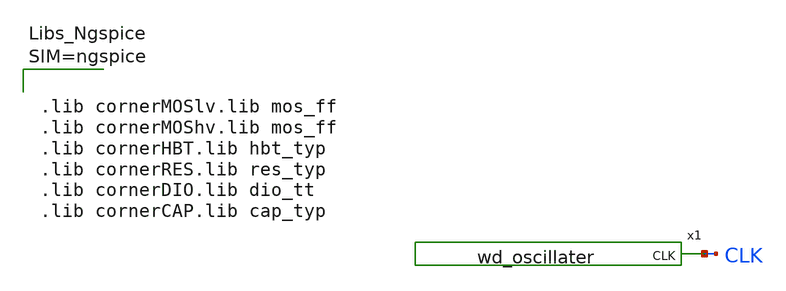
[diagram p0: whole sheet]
** sch_path: design/blocks/oscillator/schematic/wd_oscillator_tb.sch
* IHP-GmbH/IHP-Open-PDK/ihp-sg13g2/libs.tech/xschem/sg13g2_stdcells/sg13g2_buf_1.sch:
* Copyright 2023 IHP PDK Authors
* Licensed under the Apache License, Version 2.0 (the "License");
**.subckt wd_oscillator_tb
x1 CLK VDD VSS wd_oscillater
**** begin user architecture code



.lib cornerMOSlv.lib mos_ff
.lib cornerMOShv.lib mos_ff
.lib cornerHBT.lib hbt_typ
.lib cornerRES.lib res_typ
.lib cornerDIO.lib dio_tt
.lib cornerCAP.lib cap_typ






* ===== TB wd_oscillator v3 : periodo sobre VC, glitches, metaestabilidad, retry =====
.param vdd=1.2
Vsup VDD 0 PWL(0 0 10u {vdd})
Vgnd VSS 0 0
.temp 27
.option method=gear maxord=2 gmin=1e-12 itl1=500 itl4=1000 rshunt=1e12
.save v(x1.chg) v(x1.vc) v(x1.vh) v(x1.vl) i(vsup)

.control
set wr_singlescale
set wr_vecnames
set hcopydevtype = svg
echo temp vdd lvl tend_ms T_us err_pct duty_pct glitch_pct tmid_ns tstart_us dVH_mV dVL_mV IDD_uA
+ RESULT > osc_report.txt

foreach t -40 27 85
  foreach v 1.08 1.2 1.32
    alterparam vdd = $v

    * ---- nivel 1: estricto ----
    set lvl = 1
    reset
    option temp=$t reltol=5e-4 abstol=1e-12 vntol=1e-6 chgtol=1e-15
    tran 0.2u 1.2m 0 0.1u
    let tend = time[length(time)-1]

    * ---- nivel 2: intermedio ----
    if tend < 1.19e-3
      set lvl = 2
      reset
      option temp=$t reltol=2e-3 abstol=1e-11 vntol=1e-5 chgtol=1e-14
      tran 0.2u 1.2m 0 0.2u
      let tend = time[length(time)-1]
    end

    * ---- nivel 3: amplio ----
    if tend < 1.19e-3
      set lvl = 3
      reset
      option temp=$t reltol=5e-3 abstol=1e-10 vntol=1e-4 chgtol=1e-13 itl4=3000
      tran 0.2u 1.2m 0 0.2u
      let tend = time[length(time)-1]
    end

    let tend_ms = tend*1e3
    hardcopy osc_case_{$t}_{$v}.svg v(x1.vc) v(x1.vh) v(x1.vl) v(x1.chg)

    if tend < 1.19e-3
      echo $t $v $lvl $&tend_ms - - - - - - - - - ABORT >> osc_report.txt
    else
      let vm = $v/2
      * periodo sobre VC (sin glitches), 4 ciclos
      meas tran tvc  TRIG v(x1.vc)  VAL=$&vm RISE=3 TARG v(x1.vc)  VAL=$&vm RISE=7
      * mismos 4 ciclos contados sobre CHG (detecta flancos de mas)
      meas tran tchg TRIG v(x1.chg) VAL=$&vm RISE=4 TARG v(x1.chg) VAL=$&vm RISE=8
      meas tran thigh TRIG v(x1.chg) VAL=$&vm RISE=5 TARG v(x1.chg) VAL=$&vm FALL=5
      meas tran tstart WHEN v(x1.chg)=$&vm FALL=1 FROM=20u
      meas tran vcmax MAX v(x1.vc) FROM=0.6m TO=1.2m
      meas tran vcmin MIN v(x1.vc) FROM=0.6m TO=1.2m
      meas tran vh    AVG v(x1.vh) FROM=0.6m TO=1.2m
      meas tran vl    AVG v(x1.vl) FROM=0.6m TO=1.2m
      meas tran iavg  AVG i(vsup)  FROM=0.6m TO=1.2m
      let chgmid = (v(x1.chg) > 0.3*$v) & (v(x1.chg) < 0.7*$v)
      meas tran tmid INTEG chgmid FROM=0.15m TO=1.2m

      let T_us   = tvc/4*1e6
      let err    = T_us-100
      let duty   = 100*thigh/(tvc/4)
      let glitch = 100*abs(tchg-tvc)/tvc
      let tmidns = tmid*1e9
      let ts_us  = tstart*1e6
      let dvh    = (vcmax-vh)*1e3
      let dvl    = (vcmin-vl)*1e3
      let idd    = -iavg*1e6

      set res = PASS
      if abs(err) > 3
        set res = FAIL_T
      end
      if abs(duty-50) > 5
        set res = FAIL_DUTY
      end
      if ts_us > 200
        set res = FAIL_START
      end
      if abs(dvh) > 20
        set res = FAIL_VH
      end
      if abs(dvl) > 20
        set res = FAIL_VL
      end
      if idd > 15
        set res = FAIL_IDD
      end
      if tmidns > 200
        set res = FAIL_META
      end
      if glitch > 1
        set res = FAIL_GLITCH
      end
      echo $t $v $lvl $&tend_ms $&T_us $&err $&duty $&glitch $&tmidns $&ts_us $&dvh $&dvl $&idd $res
+ >> osc_report.txt
    end
  end
end
echo listo >> osc_report.txt
shell cat osc_report.txt
.endc



**** end user architecture code
**.ends

* expanding   symbol:  wd_oscillater.sym # of pins=1
** sym_path: design/blocks/oscillator/schematic/wd_oscillater.sym
** sch_path: design/blocks/oscillator/schematic/wd_oscillater.sch
.subckt wd_oscillater CLK VDD VSS
*.opin CLK
x1 net2 net1 VDD VSS bias
x2 net2 VL VC SET VDD VSS comp_inf
x3 net1 VC VH RST VDD VSS comp_sup
XR1 VDD VH VSS rhigh w=1e-6 l=150.0e-6 m=1 b=0 mm_ok=1
XR2 VH VL VSS rhigh w=1e-6 l=150.0e-6 m=1 b=0 mm_ok=1
XR3 VL VSS VSS rhigh w=1e-6 l=150.0e-6 m=1 b=0 mm_ok=1
x4 NCHG SET CHG VDD VSS sg13g2_nor2_1
x5 CHG RST NCHG VDD VSS sg13g2_nor2_1
x6 DRIVE CHG VDD VSS sg13g2_buf_1
x7 CLK CHG VDD VSS sg13g2_buf_4
XR4 VC DRIVE VSS rppd w=0.5e-6 l=175.5e-6 m=1 b=15 mm_ok=1
XC1 VH VSS cap_cmim w=20.0e-6 l=20.0e-6 m=1 mm_ok=1
XC3 VL VSS cap_cmim w=20.0e-6 l=20.0e-6 m=1 mm_ok=1
XC4 VC VSS cap_cmim w=64.0e-6 l=64.0e-6 m=8 mm_ok=1
.ends


* expanding   symbol:  bias.sym # of pins=2
** sym_path: design/blocks/bias/schematic/bias.sym
** sch_path: design/blocks/bias/schematic/bias.sch
.subckt bias VBP VBN VDD VSS
*.opin VBP
*.opin VBN
XM1 VBN VBN VSS VSS sg13_lv_nmos w=2u l=4u ng=1 m=1 mm_ok=1
XM2 VBP VBP VDD VDD sg13_lv_pmos w=4u l=4u ng=1 m=1 mm_ok=1
XR1 VDD VBN VSS rhigh w=0.5e-6 l=237.0e-6 m=1 b=0 mm_ok=1
XC1 VBN VSS cap_cmim w=26.0e-6 l=26.0e-6 m=1 mm_ok=1
XC2 VDD VBP cap_cmim w=26.0e-6 l=26.0e-6 m=1 mm_ok=1
XM3 VBP VBN VSS VSS sg13_lv_nmos w=2u l=4u ng=1 m=1 mm_ok=1
.ends


* expanding   symbol:  comp_inf.sym # of pins=4
** sym_path: design/blocks/comparator/schematic/comp_inf.sym
** sch_path: design/blocks/comparator/schematic/comp_inf.sch
.subckt comp_inf VBP VP VN OUT VDD VSS
*.opin OUT
*.ipin VN
*.ipin VP
*.ipin VBP
XM1 net3 VBP VDD VDD sg13_lv_pmos w=4u l=4u ng=1 m=1 mm_ok=1
XM7 net4 VP net3 VDD sg13_lv_pmos w=20u l=1u ng=4 m=1 mm_ok=1
XM8 net1 VN net3 VDD sg13_lv_pmos w=20u l=1u ng=4 m=1 mm_ok=1
XM9 net4 net4 VSS VSS sg13_lv_nmos w=1u l=8u ng=1 m=1 mm_ok=1
XM10 net1 net4 VSS VSS sg13_lv_nmos w=1u l=8u ng=1 m=1 mm_ok=1
XM2 net2 VBP VDD VDD sg13_lv_pmos w=4u l=4u ng=1 m=1 mm_ok=1
XM3 net2 net1 VSS VSS sg13_lv_nmos w=2u l=8u ng=1 m=1 mm_ok=1
x1 net2 OUT VDD VSS schmitt
.ends


* expanding   symbol:  comp_sup.sym # of pins=4
** sym_path: design/blocks/comparator/schematic/comp_sup.sym
** sch_path: design/blocks/comparator/schematic/comp_sup.sch
.subckt comp_sup VBN VP VN OUT VDD VSS
*.opin OUT
*.ipin VN
*.ipin VP
*.ipin VBN
XM2 net1 net1 VDD VDD sg13_lv_pmos w=2u l=4u ng=1 m=1 mm_ok=1
XM3 net3 net1 VDD VDD sg13_lv_pmos w=2u l=4u ng=1 m=1 mm_ok=1
XM4 net1 VP net2 VSS sg13_lv_nmos w=20u l=2u ng=4 m=1 mm_ok=1
XM5 net3 VN net2 VSS sg13_lv_nmos w=20u l=2u ng=4 m=1 mm_ok=1
XM6 net2 VBN VSS VSS sg13_lv_nmos w=2u l=4u ng=1 m=1 mm_ok=1
XM1 net4 net3 VDD VDD sg13_lv_pmos w=4u l=4u ng=1 m=1 mm_ok=1
XM7 net4 VBN VSS VSS sg13_lv_nmos w=2u l=4u ng=1 m=1 mm_ok=1
x1 net4 OUT VDD VSS schmitt
.ends


* expanding   symbol:  sg13g2_nor2_1.sym # of pins=3
** sym_path: sg13g2_nor2_1.sym
** sch_path: sg13g2_nor2_1.sch
.subckt sg13g2_nor2_1 Y A B VDD VSS
*.opin Y
*.ipin B
*.ipin A
*.iopin VDD
*.iopin VSS
XM1 Y A VSS VSS sg13_lv_nmos w=740.00n l=130.00n ng=1 m=1 mm_ok=1
XM2 Y B VSS VSS sg13_lv_nmos w=740.00n l=130.00n ng=1 m=1 mm_ok=1
XM3 net1 A VDD VDD sg13_lv_pmos w=1.12u l=130.00n ng=1 m=1 mm_ok=1
XM4 Y B net1 VDD sg13_lv_pmos w=1.12u l=130.00n ng=1 m=1 mm_ok=1
.ends


* expanding   symbol:  sg13g2_buf_1.sym # of pins=2
** sym_path: sg13g2_buf_1.sym
** sch_path: sg13g2_buf_1.sch
.subckt sg13g2_buf_1 X A VDD VSS
*.ipin A
*.opin X
*.iopin VDD
*.iopin VSS
XM1 net1 A VSS VSS sg13_lv_nmos w=550.00n l=130.00n ng=1 m=1 mm_ok=1
XM2 X net1 VSS VSS sg13_lv_nmos w=740.00n l=130.00n ng=1 m=1 mm_ok=1
XM3 net1 A VDD VDD sg13_lv_pmos w=840.00n l=130.00n ng=1 m=1 mm_ok=1
XM4 X net1 VDD VDD sg13_lv_pmos w=1.12u l=130.00n ng=1 m=1 mm_ok=1
.ends


* expanding   symbol:  sg13g2_buf_4.sym # of pins=2
** sym_path: sg13g2_buf_4.sym
** sch_path: sg13g2_buf_4.sch
.subckt sg13g2_buf_4 X A VDD VSS
*.ipin A
*.opin X
*.iopin VDD
*.iopin VSS
XM1 net1 A VSS VSS sg13_lv_nmos w=740.00n l=130.00n ng=1 m=1 mm_ok=1
XM2 X net1 VSS VSS sg13_lv_nmos w=2.96u l=130.00n ng=4 m=1 mm_ok=1
XM3 net1 A VDD VDD sg13_lv_pmos w=1.68u l=130.00n ng=2 m=1 mm_ok=1
XM4 X net1 VDD VDD sg13_lv_pmos w=4.48u l=130.00n ng=4 m=1 mm_ok=1
.ends


* expanding   symbol:  schmitt.sym # of pins=2
** sym_path: design/blocks/schmitt/schematic/schmitt.sym
** sch_path: design/blocks/schmitt/schematic/schmitt.sch
.subckt schmitt IN OUT VDD VSS
*.opin OUT
*.ipin IN
XM4 net1 IN VDD VDD sg13_lv_pmos w=1.04u l=0.13u ng=1 m=1 mm_ok=1
XM6 OUT IN net2 VSS sg13_lv_nmos w=0.76u l=0.13u ng=1 m=1 mm_ok=1
XM5 OUT IN net1 VDD sg13_lv_pmos w=1.04u l=0.13u ng=1 m=1 mm_ok=1
XM7 net2 IN VSS VSS sg13_lv_nmos w=0.76u l=0.13u ng=1 m=1 mm_ok=1
XM8 VSS OUT net1 VDD sg13_lv_pmos w=0.42u l=0.13u ng=1 m=1 mm_ok=1
XM9 VDD OUT net2 VSS sg13_lv_nmos w=0.42u l=0.13u ng=1 m=1 mm_ok=1
.ends

.end
